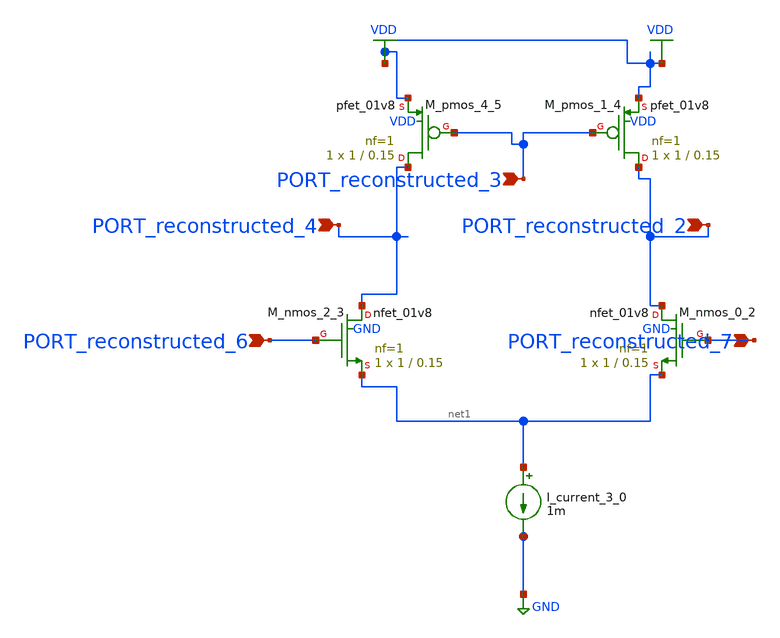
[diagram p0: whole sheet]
** sch_path: schematics/Image2Net/033.sch
**.subckt 033 PORT_reconstructed_3 PORT_reconstructed_4 PORT_reconstructed_6 PORT_reconstructed_2
*+ PORT_reconstructed_7
*.ipin PORT_reconstructed_3
*.ipin PORT_reconstructed_4
*.ipin PORT_reconstructed_6
*.ipin PORT_reconstructed_2
*.ipin PORT_reconstructed_7
I_current_3_0 net1 GND 1m
XM_nmos_0_2 PORT_reconstructed_2 PORT_reconstructed_7 net1 GND sky130_fd_pr__nfet_01v8 L=0.15 W=1 nf=1
+ ad='int((1 + 1)/2) * 1 / 1 * 0.29' as='int((1 + 2)/2) * 1 / 1 * 0.29' pd='2*int((1 + 1)/2) * (1 / 1 + 0.29)'
+ ps='2*int((1 + 2)/2) * (1 / 1 + 0.29)' nrd='0.29 / 1 ' nrs='0.29 / 1 ' sa=0 sb=0 sd=0 mult=1 m=1
XM_nmos_2_3 PORT_reconstructed_4 PORT_reconstructed_6 net1 GND sky130_fd_pr__nfet_01v8 L=0.15 W=1 nf=1
+ ad='int((1 + 1)/2) * 1 / 1 * 0.29' as='int((1 + 2)/2) * 1 / 1 * 0.29' pd='2*int((1 + 1)/2) * (1 / 1 + 0.29)'
+ ps='2*int((1 + 2)/2) * (1 / 1 + 0.29)' nrd='0.29 / 1 ' nrs='0.29 / 1 ' sa=0 sb=0 sd=0 mult=1 m=1
XM_pmos_1_4 PORT_reconstructed_2 PORT_reconstructed_3 VDD VDD sky130_fd_pr__pfet_01v8 L=0.15 W=1 nf=1
+ ad='int((1 + 1)/2) * 1 / 1 * 0.29' as='int((1 + 2)/2) * 1 / 1 * 0.29' pd='2*int((1 + 1)/2) * (1 / 1 + 0.29)'
+ ps='2*int((1 + 2)/2) * (1 / 1 + 0.29)' nrd='0.29 / 1 ' nrs='0.29 / 1 ' sa=0 sb=0 sd=0 mult=1 m=1
XM_pmos_4_5 PORT_reconstructed_4 PORT_reconstructed_3 VDD VDD sky130_fd_pr__pfet_01v8 L=0.15 W=1 nf=1
+ ad='int((1 + 1)/2) * 1 / 1 * 0.29' as='int((1 + 2)/2) * 1 / 1 * 0.29' pd='2*int((1 + 1)/2) * (1 / 1 + 0.29)'
+ ps='2*int((1 + 2)/2) * (1 / 1 + 0.29)' nrd='0.29 / 1 ' nrs='0.29 / 1 ' sa=0 sb=0 sd=0 mult=1 m=1
**.ends
.GLOBAL GND
.GLOBAL VDD
.end
